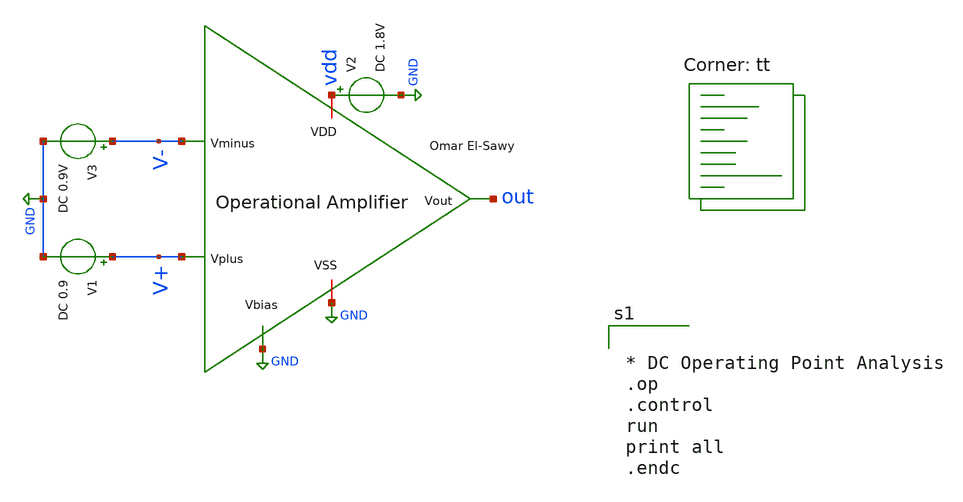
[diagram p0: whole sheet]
** sch_path: analog/library/Operational_Amplifiers/TemplateBenches/DifferentialGain.sch
**.subckt DifferentialGain
x1 vdd out V- V+ GND GND OpAmp
V1 V+ GND DC 0.9
V3 V- GND DC 0.9V
V2 vdd GND DC 1.8V
**** begin user architecture code


* DC Operating Point Analysis
.op
.control
run
print all
.endc


.lib $::SKYWATER_MODELS/sky130.lib.spice tt
**** end user architecture code
**.ends

* expanding   symbol:  Operational_Amplifiers/OpAmp.sym # of pins=6
** sym_path: Operational_Amplifiers/OpAmp.sym
** sch_path: Operational_Amplifiers/OpAmp.sch
.subckt OpAmp VDD Vout Vminus Vplus Vbias VSS
*.ipin Vbias
*.ipin Vplus
*.ipin Vminus
*.opin Vout
*.iopin VDD
*.iopin VSS
XM1 net2 Vminus net1 VSS sky130_fd_pr__nfet_01v8 L=0.15 W=10 nf=1 ad='int((nf+1)/2) * W/nf * 0.29' as='int((nf+2)/2) * W/nf * 0.29'
+ pd='2*int((nf+1)/2) * (W/nf + 0.29)' ps='2*int((nf+2)/2) * (W/nf + 0.29)' nrd='0.29 / W' nrs='0.29 / W'
+ sa=0 sb=0 sd=0 mult=1 m=1
XM2 V1st Vplus net1 VSS sky130_fd_pr__nfet_01v8 L=0.15 W=10 nf=1 ad='int((nf+1)/2) * W/nf * 0.29' as='int((nf+2)/2) * W/nf * 0.29'
+ pd='2*int((nf+1)/2) * (W/nf + 0.29)' ps='2*int((nf+2)/2) * (W/nf + 0.29)' nrd='0.29 / W' nrs='0.29 / W'
+ sa=0 sb=0 sd=0 mult=1 m=1
XM3 net1 Vbias VSS VSS sky130_fd_pr__nfet_01v8 L=0.3 W=15 nf=1 ad='int((nf+1)/2) * W/nf * 0.29' as='int((nf+2)/2) * W/nf * 0.29'
+ pd='2*int((nf+1)/2) * (W/nf + 0.29)' ps='2*int((nf+2)/2) * (W/nf + 0.29)' nrd='0.29 / W' nrs='0.29 / W'
+ sa=0 sb=0 sd=0 mult=1 m=1
XM4 net2 net2 VDD VDD sky130_fd_pr__pfet_01v8 L=0.15 W=5 nf=1 ad='int((nf+1)/2) * W/nf * 0.29' as='int((nf+2)/2) * W/nf * 0.29'
+ pd='2*int((nf+1)/2) * (W/nf + 0.29)' ps='2*int((nf+2)/2) * (W/nf + 0.29)' nrd='0.29 / W' nrs='0.29 / W'
+ sa=0 sb=0 sd=0 mult=1 m=1
XM5 V1st net2 VDD VDD sky130_fd_pr__pfet_01v8 L=0.15 W=5 nf=1 ad='int((nf+1)/2) * W/nf * 0.29' as='int((nf+2)/2) * W/nf * 0.29'
+ pd='2*int((nf+1)/2) * (W/nf + 0.29)' ps='2*int((nf+2)/2) * (W/nf + 0.29)' nrd='0.29 / W' nrs='0.29 / W'
+ sa=0 sb=0 sd=0 mult=1 m=1
XM6 Vout V1st VDD VDD sky130_fd_pr__pfet_01v8 L=0.15 W=20 nf=1 ad='int((nf+1)/2) * W/nf * 0.29' as='int((nf+2)/2) * W/nf * 0.29'
+ pd='2*int((nf+1)/2) * (W/nf + 0.29)' ps='2*int((nf+2)/2) * (W/nf + 0.29)' nrd='0.29 / W' nrs='0.29 / W'
+ sa=0 sb=0 sd=0 mult=1 m=1
XM7 Vout Vbias VSS VSS sky130_fd_pr__nfet_01v8 L=0.15 W=10 nf=1 ad='int((nf+1)/2) * W/nf * 0.29' as='int((nf+2)/2) * W/nf * 0.29'
+ pd='2*int((nf+1)/2) * (W/nf + 0.29)' ps='2*int((nf+2)/2) * (W/nf + 0.29)' nrd='0.29 / W' nrs='0.29 / W'
+ sa=0 sb=0 sd=0 mult=1 m=1
XC2 Vout V1st sky130_fd_pr__cap_mim_m3_2 W=12 L=1 MF=12 m=12
.ends

.GLOBAL GND
.GLOBAL VSS
.GLOBAL VDD
.end
